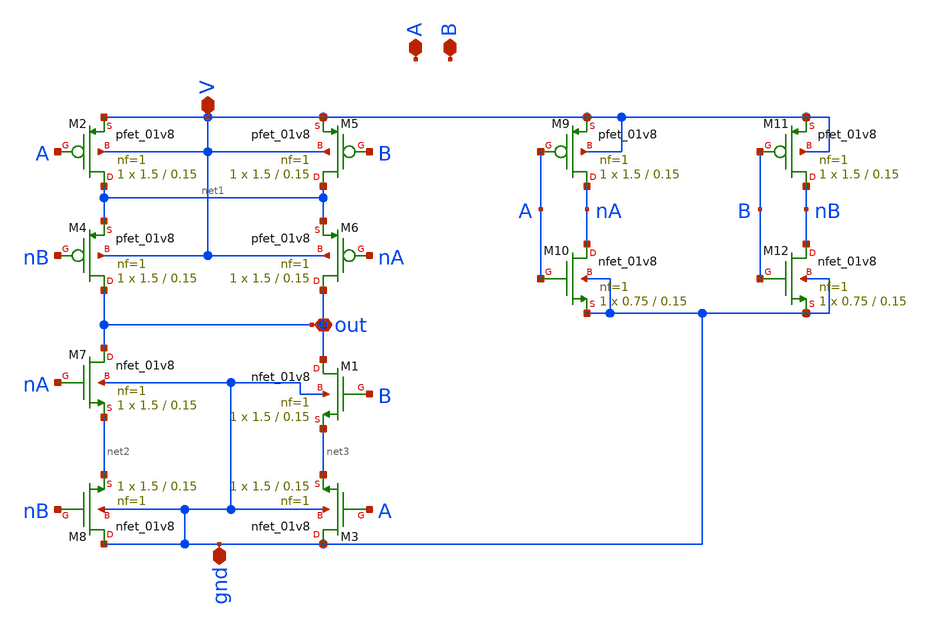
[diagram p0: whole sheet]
** sch_path: xschem/designs/counter4b/xor_gate.sch
**.subckt xor_gate A out gnd V B
*.iopin A
*.iopin out
*.iopin gnd
*.iopin V
*.iopin B
XM1 out B net3 gnd sky130_fd_pr__nfet_01v8 L=0.15 W=1.5 nf=1 ad='int((nf+1)/2) * W/nf * 0.29' as='int((nf+2)/2) * W/nf * 0.29'
+ pd='2*int((nf+1)/2) * (W/nf + 0.29)' ps='2*int((nf+2)/2) * (W/nf + 0.29)' nrd='0.29 / W' nrs='0.29 / W'
+ sa=0 sb=0 sd=0 mult=1 m=1
XM2 net1 A V V sky130_fd_pr__pfet_01v8 L=0.15 W=1.5 nf=1 ad='int((nf+1)/2) * W/nf * 0.29' as='int((nf+2)/2) * W/nf * 0.29'
+ pd='2*int((nf+1)/2) * (W/nf + 0.29)' ps='2*int((nf+2)/2) * (W/nf + 0.29)' nrd='0.29 / W' nrs='0.29 / W'
+ sa=0 sb=0 sd=0 mult=1 m=1
XM3 gnd A net3 gnd sky130_fd_pr__nfet_01v8 L=0.15 W=1.5 nf=1 ad='int((nf+1)/2) * W/nf * 0.29' as='int((nf+2)/2) * W/nf * 0.29'
+ pd='2*int((nf+1)/2) * (W/nf + 0.29)' ps='2*int((nf+2)/2) * (W/nf + 0.29)' nrd='0.29 / W' nrs='0.29 / W'
+ sa=0 sb=0 sd=0 mult=1 m=1
XM4 out nB net1 V sky130_fd_pr__pfet_01v8 L=0.15 W=1.5 nf=1 ad='int((nf+1)/2) * W/nf * 0.29' as='int((nf+2)/2) * W/nf * 0.29'
+ pd='2*int((nf+1)/2) * (W/nf + 0.29)' ps='2*int((nf+2)/2) * (W/nf + 0.29)' nrd='0.29 / W' nrs='0.29 / W'
+ sa=0 sb=0 sd=0 mult=1 m=1
XM5 net1 B V V sky130_fd_pr__pfet_01v8 L=0.15 W=1.5 nf=1 ad='int((nf+1)/2) * W/nf * 0.29' as='int((nf+2)/2) * W/nf * 0.29'
+ pd='2*int((nf+1)/2) * (W/nf + 0.29)' ps='2*int((nf+2)/2) * (W/nf + 0.29)' nrd='0.29 / W' nrs='0.29 / W'
+ sa=0 sb=0 sd=0 mult=1 m=1
XM6 out nA net1 V sky130_fd_pr__pfet_01v8 L=0.15 W=1.5 nf=1 ad='int((nf+1)/2) * W/nf * 0.29' as='int((nf+2)/2) * W/nf * 0.29'
+ pd='2*int((nf+1)/2) * (W/nf + 0.29)' ps='2*int((nf+2)/2) * (W/nf + 0.29)' nrd='0.29 / W' nrs='0.29 / W'
+ sa=0 sb=0 sd=0 mult=1 m=1
XM7 out nA net2 gnd sky130_fd_pr__nfet_01v8 L=0.15 W=1.5 nf=1 ad='int((nf+1)/2) * W/nf * 0.29' as='int((nf+2)/2) * W/nf * 0.29'
+ pd='2*int((nf+1)/2) * (W/nf + 0.29)' ps='2*int((nf+2)/2) * (W/nf + 0.29)' nrd='0.29 / W' nrs='0.29 / W'
+ sa=0 sb=0 sd=0 mult=1 m=1
XM8 gnd nB net2 gnd sky130_fd_pr__nfet_01v8 L=0.15 W=1.5 nf=1 ad='int((nf+1)/2) * W/nf * 0.29' as='int((nf+2)/2) * W/nf * 0.29'
+ pd='2*int((nf+1)/2) * (W/nf + 0.29)' ps='2*int((nf+2)/2) * (W/nf + 0.29)' nrd='0.29 / W' nrs='0.29 / W'
+ sa=0 sb=0 sd=0 mult=1 m=1
XM9 nA A V V sky130_fd_pr__pfet_01v8 L=0.15 W=1.5 nf=1 ad='int((nf+1)/2) * W/nf * 0.29' as='int((nf+2)/2) * W/nf * 0.29'
+ pd='2*int((nf+1)/2) * (W/nf + 0.29)' ps='2*int((nf+2)/2) * (W/nf + 0.29)' nrd='0.29 / W' nrs='0.29 / W'
+ sa=0 sb=0 sd=0 mult=1 m=1
XM10 nA A gnd gnd sky130_fd_pr__nfet_01v8 L=0.15 W=0.75 nf=1 ad='int((nf+1)/2) * W/nf * 0.29' as='int((nf+2)/2) * W/nf * 0.29'
+ pd='2*int((nf+1)/2) * (W/nf + 0.29)' ps='2*int((nf+2)/2) * (W/nf + 0.29)' nrd='0.29 / W' nrs='0.29 / W'
+ sa=0 sb=0 sd=0 mult=1 m=1
XM11 nB B V V sky130_fd_pr__pfet_01v8 L=0.15 W=1.5 nf=1 ad='int((nf+1)/2) * W/nf * 0.29' as='int((nf+2)/2) * W/nf * 0.29'
+ pd='2*int((nf+1)/2) * (W/nf + 0.29)' ps='2*int((nf+2)/2) * (W/nf + 0.29)' nrd='0.29 / W' nrs='0.29 / W'
+ sa=0 sb=0 sd=0 mult=1 m=1
XM12 nB B gnd gnd sky130_fd_pr__nfet_01v8 L=0.15 W=0.75 nf=1 ad='int((nf+1)/2) * W/nf * 0.29' as='int((nf+2)/2) * W/nf * 0.29'
+ pd='2*int((nf+1)/2) * (W/nf + 0.29)' ps='2*int((nf+2)/2) * (W/nf + 0.29)' nrd='0.29 / W' nrs='0.29 / W'
+ sa=0 sb=0 sd=0 mult=1 m=1
**.ends
.end
